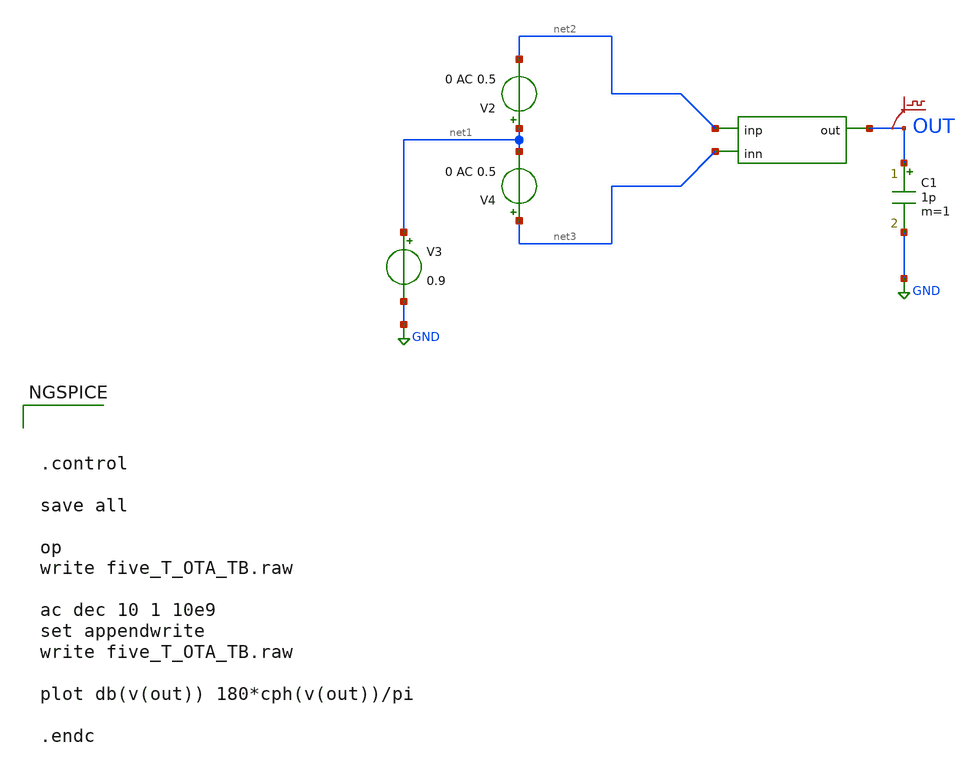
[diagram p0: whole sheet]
** sch_path: archive/q2_opamp_tb.sch
**.subckt q2_opamp_tb
V2 net1 net2 0 AC 0.5
V3 net1 GND 0.9
C1 OUT GND 1p m=1
.save v(out)
V4 net3 net1 0 AC 0.5
**** begin user architecture code



.control

save all

op
write five_T_OTA_TB.raw

ac dec 10 1 10e9
set appendwrite
write five_T_OTA_TB.raw

plot db(v(out)) 180*cph(v(out))/pi

.endc



** opencircuitdesign pdks install
.lib $::SKYWATER_MODELS/sky130.lib.spice tt


**** end user architecture code
**.ends
.GLOBAL GND
.end
